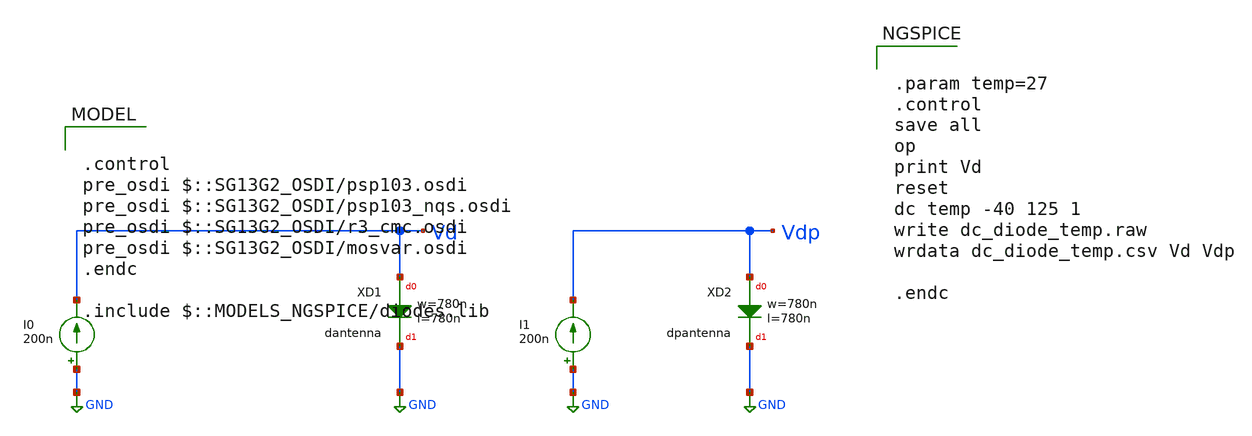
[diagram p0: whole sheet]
** sch_path: ihp-sg13g2/xschem_libs/sg13g2_tests/dc_diode_temp/schematic/dc_diode_temp.sch
* Copyright 2023 IHP PDK Authors
**.subckt dc_diode_temp
XXD1 Vd GND dantenna l=780n w=780n
I0 GND Vd 200n
I1 GND Vdp 200n
XXD2 Vdp GND dpantenna l=780n w=780n
**** begin user architecture code

.control
pre_osdi $::SG13G2_OSDI/psp103.osdi
pre_osdi $::SG13G2_OSDI/psp103_nqs.osdi
pre_osdi $::SG13G2_OSDI/r3_cmc.osdi
pre_osdi $::SG13G2_OSDI/mosvar.osdi
.endc

.include $::MODELS_NGSPICE/diodes.lib



.param temp=27
.control
save all
op
print Vd
reset
dc temp -40 125 1
write dc_diode_temp.raw
wrdata dc_diode_temp.csv Vd Vdp

.endc


**** end user architecture code
**.ends
.GLOBAL GND
.end
